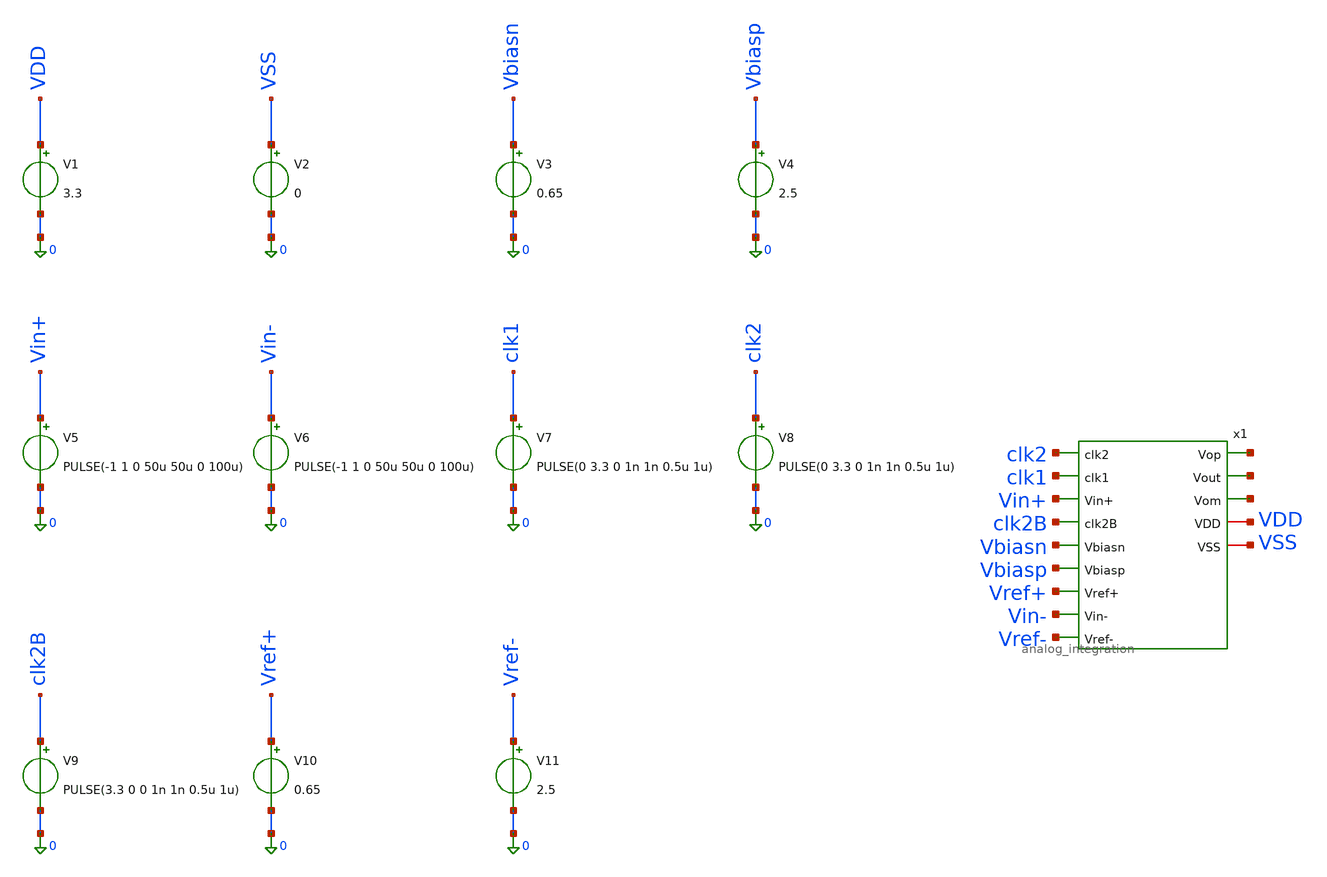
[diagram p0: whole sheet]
** sch_path: src/schematics/INTEGRATION/analog_integration_tb.sch
**.subckt analog_integration_tb
x1 clk2 clk1 Vin+ net1 net2 net3 clk2B Vbiasn Vbiasp VDD Vref+ Vin- Vref- VSS analog_integration
V1 VDD 0 3.3
V2 VSS 0 0
V3 Vbiasn 0 0.65
V4 Vbiasp 0 2.5
V5 Vin+ 0 PULSE(-1 1 0 50u 50u 0 100u)
V6 Vin- 0 PULSE(-1 1 0 50u 50u 0 100u)
V7 clk1 0 PULSE(0 3.3 0 1n 1n 0.5u 1u)
V8 clk2 0 PULSE(0 3.3 0 1n 1n 0.5u 1u)
V9 clk2B 0 PULSE(3.3 0 0 1n 1n 0.5u 1u)
V10 Vref+ 0 0.65
V11 Vref- 0 2.5
**.ends
.end
